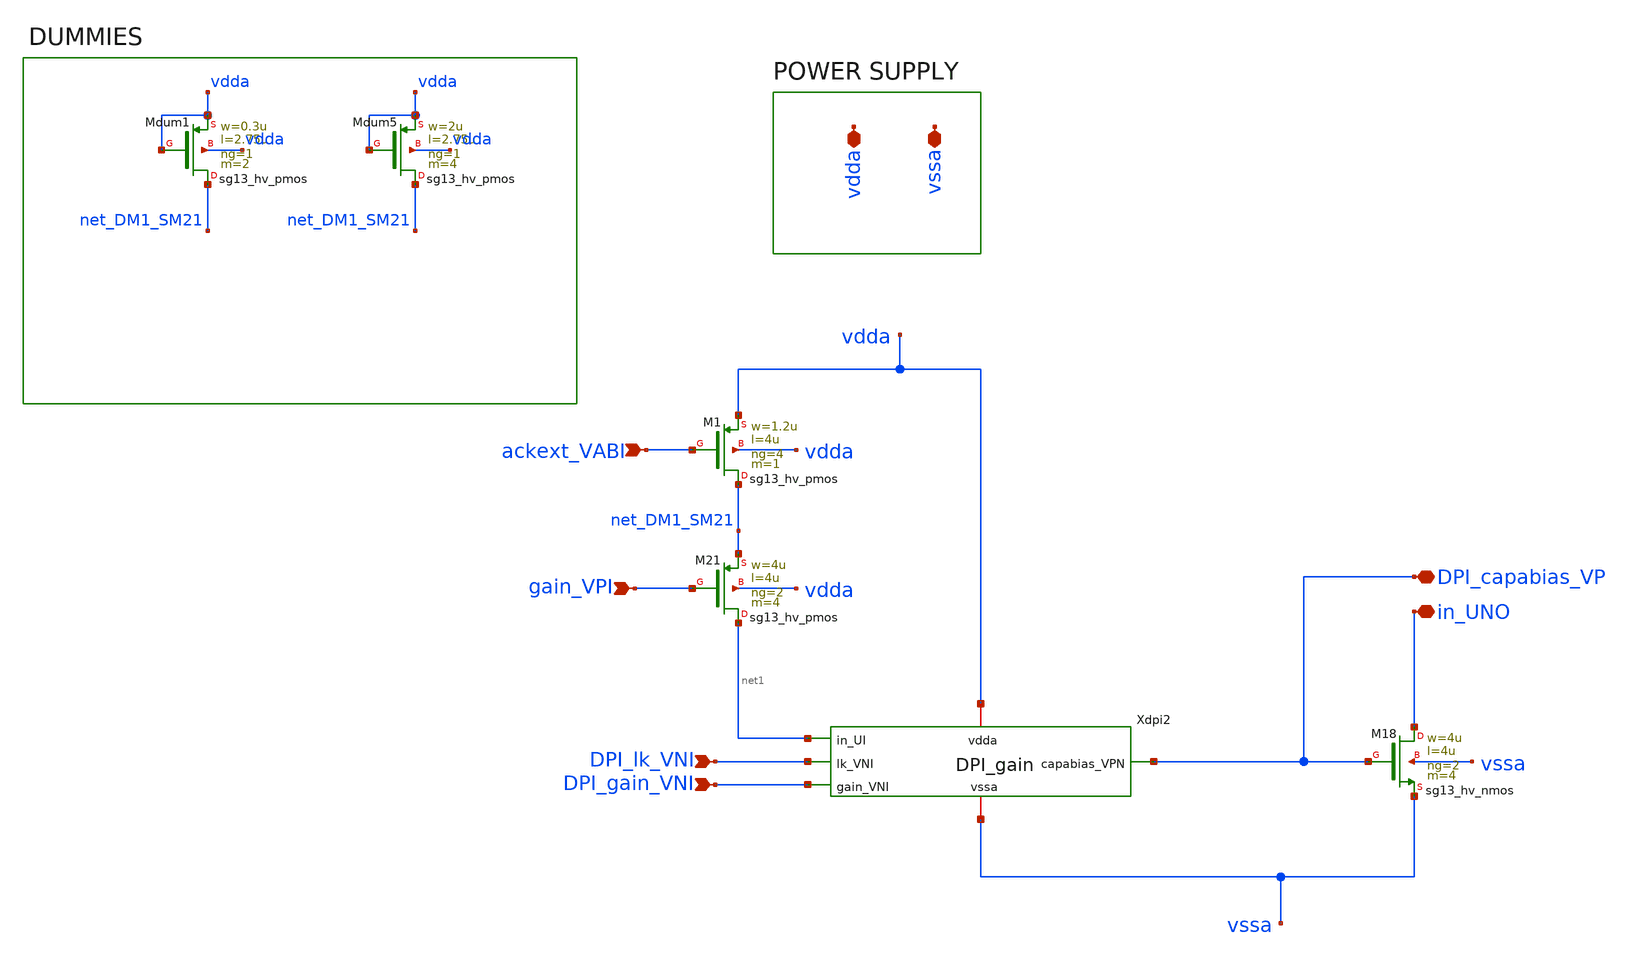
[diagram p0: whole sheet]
** sch_path: ADAP_system.sch
**.subckt ADAP_system ackext_VABI gain_VPI DPI_gain_VNI DPI_lk_VNI vssa vdda DPI_capabias_VP in_UNO
*.ipin ackext_VABI
*.ipin gain_VPI
*.ipin DPI_gain_VNI
*.ipin DPI_lk_VNI
*.iopin vssa
*.iopin vdda
*.iopin DPI_capabias_VP
*.iopin in_UNO
XM21 net1 gain_VPI net_DM1_SM21 vdda sg13_hv_pmos w=4u l=4u ng=2 m=4 mm_ok=1
XM18 in_UNO DPI_capabias_VP vssa vssa sg13_hv_nmos w=4u l=4u ng=2 m=4 mm_ok=1
XM1 net_DM1_SM21 ackext_VABI vdda vdda sg13_hv_pmos w=1.2u l=4u ng=4 m=1 mm_ok=1
Xdpi2 net1 vdda DPI_capabias_VP DPI_gain_VNI vssa DPI_lk_VNI DPI_gain
XMdum5 net_DM1_SM21 vdda vdda vdda sg13_hv_pmos w=2u l=2.75u ng=1 m=4 mm_ok=1
XMdum1 net_DM1_SM21 vdda vdda vdda sg13_hv_pmos w=0.3u l=2.75u ng=1 m=2 mm_ok=1
**.ends

* expanding   symbol:  DPI_gain.sym # of pins=6
** sym_path: DPI_gain.sym
** sch_path: DPI_gain.sch
.subckt DPI_gain in_UI vdda capabias_VPN gain_VNI vssa lk_VNI
*.ipin gain_VNI
*.ipin lk_VNI
*.iopin capabias_VPN
*.iopin vssa
*.iopin vdda
*.iopin in_UI
XMdifl vssa gain_VNI in_UI vdda sg13_hv_pmos w=2u l=2u ng=2 m=8 mm_ok=1
XMdifr capabias_VPN capabias_VPN in_UI vdda sg13_hv_pmos w=2u l=2u ng=2 m=8 mm_ok=1
XMtau capabias_VPN lk_VNI vssa vssa sg13_hv_nmos w=4u l=4u ng=2 m=4 mm_ok=1
XMdum2 in_UI vdda vdda vdda sg13_hv_pmos w=1u l=2u ng=1 m=8 mm_ok=1
.ends

.end
